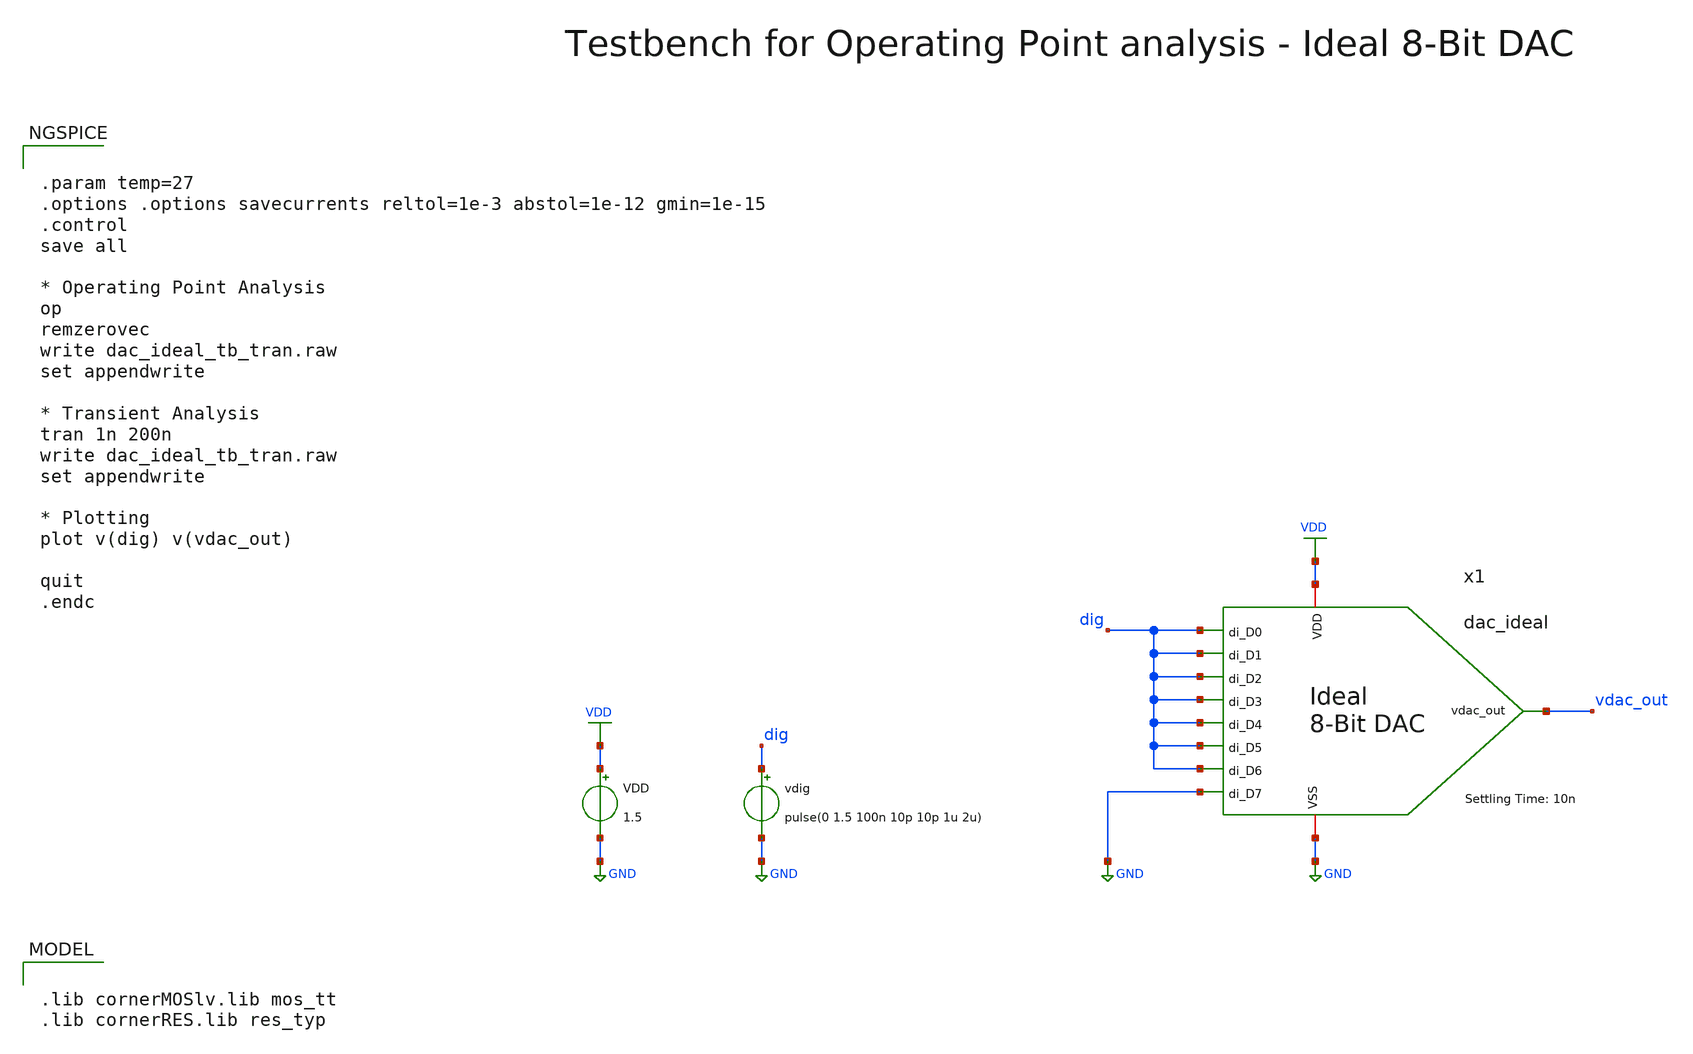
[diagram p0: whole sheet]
** sch_path: SG13G2_ATBS-ADC-main/xschem/dac/ideal/testbenches/dac_ideal_tb_tran.sch
**.subckt dac_ideal_tb_tran
VDD VDD GND 1.5
vdig dig GND pulse(0 1.5 100n 10p 10p 1u 2u)
x1 VDD dig dig dig dig dig GND dig dig vdac_out GND dac_ideal tsettle=10n
**** begin user architecture code

.lib cornerMOSlv.lib mos_tt
.lib cornerRES.lib res_typ



.param temp=27
.options .options savecurrents reltol=1e-3 abstol=1e-12 gmin=1e-15
.control
save all

* Operating Point Analysis
op
remzerovec
write dac_ideal_tb_tran.raw
set appendwrite

* Transient Analysis
tran 1n 200n
write dac_ideal_tb_tran.raw
set appendwrite

* Plotting
plot v(dig) v(vdac_out)

quit
.endc

**** end user architecture code
**.ends

* expanding   symbol:  dac/ideal/dac_ideal.sym # of pins=11
** sym_path: SG13G2_ATBS-ADC-main/xschem/dac/ideal/dac_ideal.sym
** sch_path: SG13G2_ATBS-ADC-main/xschem/dac/ideal/dac_ideal.sch
.subckt dac_ideal VDD di_D1 di_D4 di_D0 di_D2 di_D3 di_D7 di_D5 di_D6 vdac_out VSS  tsettle=10n
*.opin vdac_out
*.ipin di_D0
*.iopin VSS
*.iopin VDD
*.ipin di_D1
*.ipin di_D2
*.ipin di_D3
*.ipin di_D4
*.ipin di_D5
*.ipin di_D6
*.ipin di_D7
R1 net1 VSS 3925 m=1
G1 VDD net1 di_D0 VSS 1u
G2 VDD net1 di_D1 VSS 2u
G3 VDD net1 di_D2 VSS 4u
G4 VDD net1 di_D3 VSS 8u
G5 VDD net1 di_D4 VSS 16u
G6 VDD net1 di_D5 VSS 32u
G7 VDD net1 di_D6 VSS 64u
G8 VDD net1 di_D7 VSS 128u
A1 net1 vdac_out VSS del_subckt
.model del_subckt delay(delay=tsettle buffer_size=8192)
.ends

.GLOBAL GND
.GLOBAL VDD
.end
